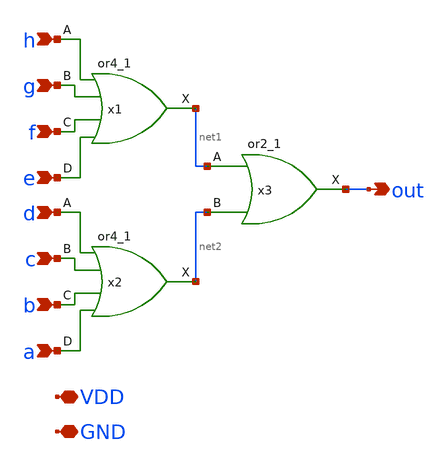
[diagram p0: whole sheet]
** sch_path: design/xschem/or8.sch
**.subckt or8 a b c d e f g h out VDD GND
*.ipin a
*.ipin b
*.ipin c
*.ipin d
*.ipin e
*.ipin f
*.ipin g
*.ipin h
*.opin out
*.iopin VDD
*.iopin GND
x1 h g f e GND GND VDD VDD net1 sky130_fd_sc_hd__or4_1
x2 d c b a GND GND VDD VDD net2 sky130_fd_sc_hd__or4_1
x3 net1 net2 GND GND VDD VDD out sky130_fd_sc_hd__or2_1
**.ends
.end
